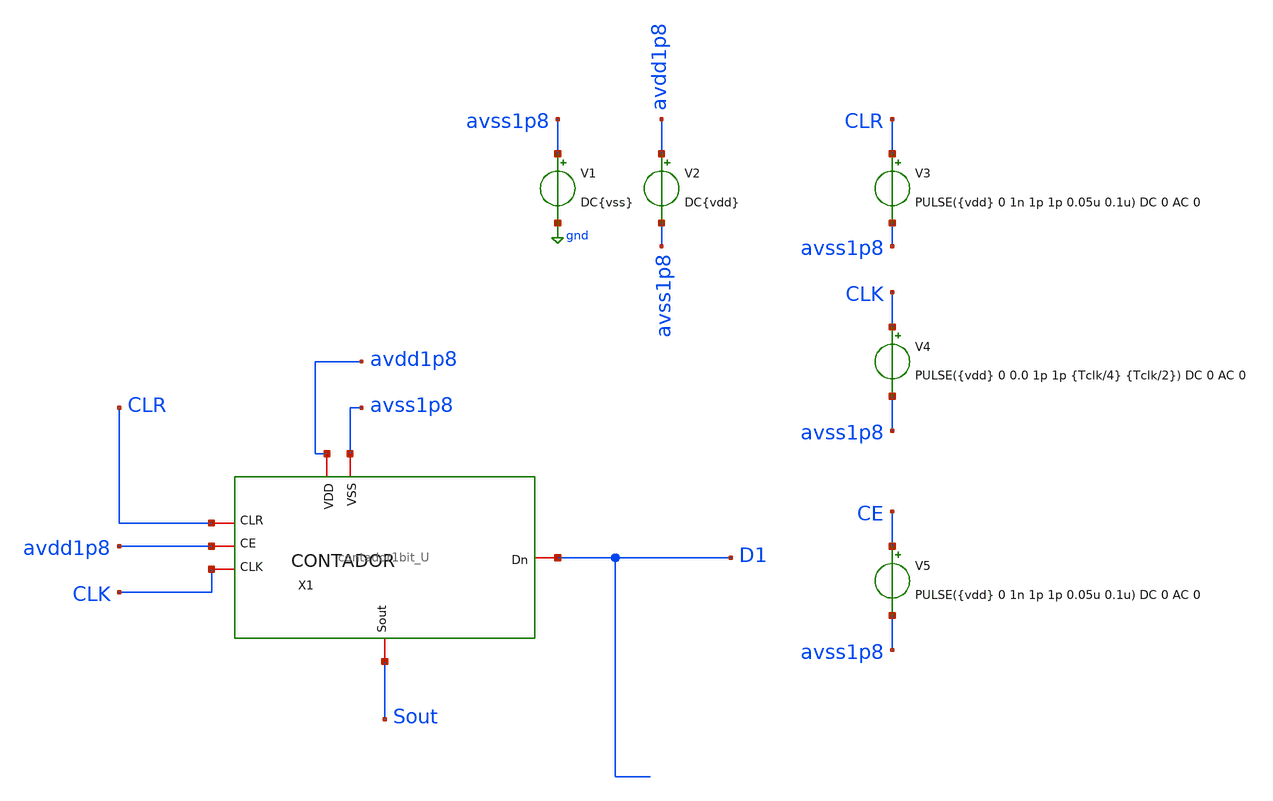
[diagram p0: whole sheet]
** sch_path: verification/testbenches/tb_contador1bit_U.sch
**.subckt tb_contador1bit_U
V1 avss1p8 gnd DC{vss}
V2 avdd1p8 avss1p8 DC{vdd}
V3 CLR avss1p8 PULSE({vdd} 0 1n 1p 1p 0.05u 0.1u) DC 0 AC 0
V4 CLK avss1p8 PULSE({vdd} 0 0.0 1p 1p {Tclk/4} {Tclk/2}) DC 0 AC 0
V5 CE avss1p8 PULSE({vdd} 0 1n 1p 1p 0.05u 0.1u) DC 0 AC 0
x1 avdd1p8 avss1p8 avdd1p8 CLR D1 CLK Sout contador1bit_U
**** begin user architecture code


* Circuit Parameters
.param vdd = 1.2
.param vss = 0.0
.param Tclk = 10n
.options TEMP = 27.0
* Include Models - IHP SG13G2
.lib cornerMOSlv.lib mos_tt
* OP Parameters & Singals to save
.save all
*Simulations
.control
tran 0.01u 100n
setplot tran1
plot v(Sout) v(D1)+1.2 v(CLK)+2.4 v(CLR)+3.6 V(CE)+4.8
reset
set filetype = ascii
write dcsweep.raw
.endc
.end


**** end user architecture code
**.ends
.GLOBAL gnd
.end
